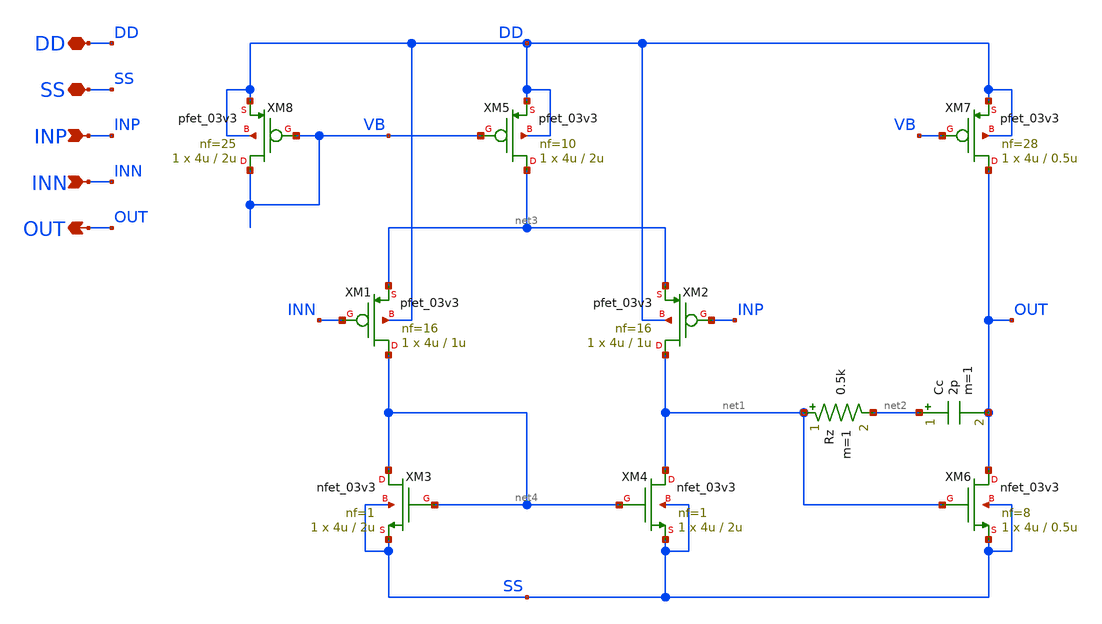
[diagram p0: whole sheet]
** sch_path: Design_Files/IC Design/Schematic/Single_ended_OTA/Single_ended_OTA.sch
**.subckt Single_ended_OTA DD SS INP INN OUT
*.iopin DD
*.iopin SS
*.ipin INP
*.ipin INN
*.opin OUT
XM4 net1 net4 SS SS nfet_03v3 L=2u W=4u nf=1 ad='int((nf+1)/2) * W/nf * 0.18u' as='int((nf+2)/2) * W/nf * 0.18u'
+ pd='2*int((nf+1)/2) * (W/nf + 0.18u)' ps='2*int((nf+2)/2) * (W/nf + 0.18u)' nrd='0.18u / W' nrs='0.18u / W'
+ sa=0 sb=0 sd=0 m=1
XM3 net4 net4 SS SS nfet_03v3 L=2u W=4u nf=1 ad='int((nf+1)/2) * W/nf * 0.18u' as='int((nf+2)/2) * W/nf * 0.18u'
+ pd='2*int((nf+1)/2) * (W/nf + 0.18u)' ps='2*int((nf+2)/2) * (W/nf + 0.18u)' nrd='0.18u / W' nrs='0.18u / W'
+ sa=0 sb=0 sd=0 m=1
XM1 net4 INN net3 DD pfet_03v3 L=1u W=4u nf=16 ad='int((nf+1)/2) * W/nf * 0.18u' as='int((nf+2)/2) * W/nf * 0.18u'
+ pd='2*int((nf+1)/2) * (W/nf + 0.18u)' ps='2*int((nf+2)/2) * (W/nf + 0.18u)' nrd='0.18u / W' nrs='0.18u / W'
+ sa=0 sb=0 sd=0 m=1
XM2 net1 INP net3 DD pfet_03v3 L=1u W=4u nf=16 ad='int((nf+1)/2) * W/nf * 0.18u' as='int((nf+2)/2) * W/nf * 0.18u'
+ pd='2*int((nf+1)/2) * (W/nf + 0.18u)' ps='2*int((nf+2)/2) * (W/nf + 0.18u)' nrd='0.18u / W' nrs='0.18u / W'
+ sa=0 sb=0 sd=0 m=1
XM7 OUT VB DD DD pfet_03v3 L=0.5u W=4u nf=28 ad='int((nf+1)/2) * W/nf * 0.18u' as='int((nf+2)/2) * W/nf * 0.18u'
+ pd='2*int((nf+1)/2) * (W/nf + 0.18u)' ps='2*int((nf+2)/2) * (W/nf + 0.18u)' nrd='0.18u / W' nrs='0.18u / W'
+ sa=0 sb=0 sd=0 m=1
Rz net1 net2 0.5k m=1
XM5 net3 VB DD DD pfet_03v3 L=2u W=4u nf=10 ad='int((nf+1)/2) * W/nf * 0.18u' as='int((nf+2)/2) * W/nf * 0.18u'
+ pd='2*int((nf+1)/2) * (W/nf + 0.18u)' ps='2*int((nf+2)/2) * (W/nf + 0.18u)' nrd='0.18u / W' nrs='0.18u / W'
+ sa=0 sb=0 sd=0 m=1
XM6 OUT net1 SS SS nfet_03v3 L=0.5u W=4u nf=8 ad='int((nf+1)/2) * W/nf * 0.18u' as='int((nf+2)/2) * W/nf * 0.18u'
+ pd='2*int((nf+1)/2) * (W/nf + 0.18u)' ps='2*int((nf+2)/2) * (W/nf + 0.18u)' nrd='0.18u / W' nrs='0.18u / W'
+ sa=0 sb=0 sd=0 m=1
XM8 VB VB DD DD pfet_03v3 L=2u W=4u nf=25 ad='int((nf+1)/2) * W/nf * 0.18u' as='int((nf+2)/2) * W/nf * 0.18u'
+ pd='2*int((nf+1)/2) * (W/nf + 0.18u)' ps='2*int((nf+2)/2) * (W/nf + 0.18u)' nrd='0.18u / W' nrs='0.18u / W'
+ sa=0 sb=0 sd=0 m=1
Cc net2 OUT 2p m=1
**.ends
.end
